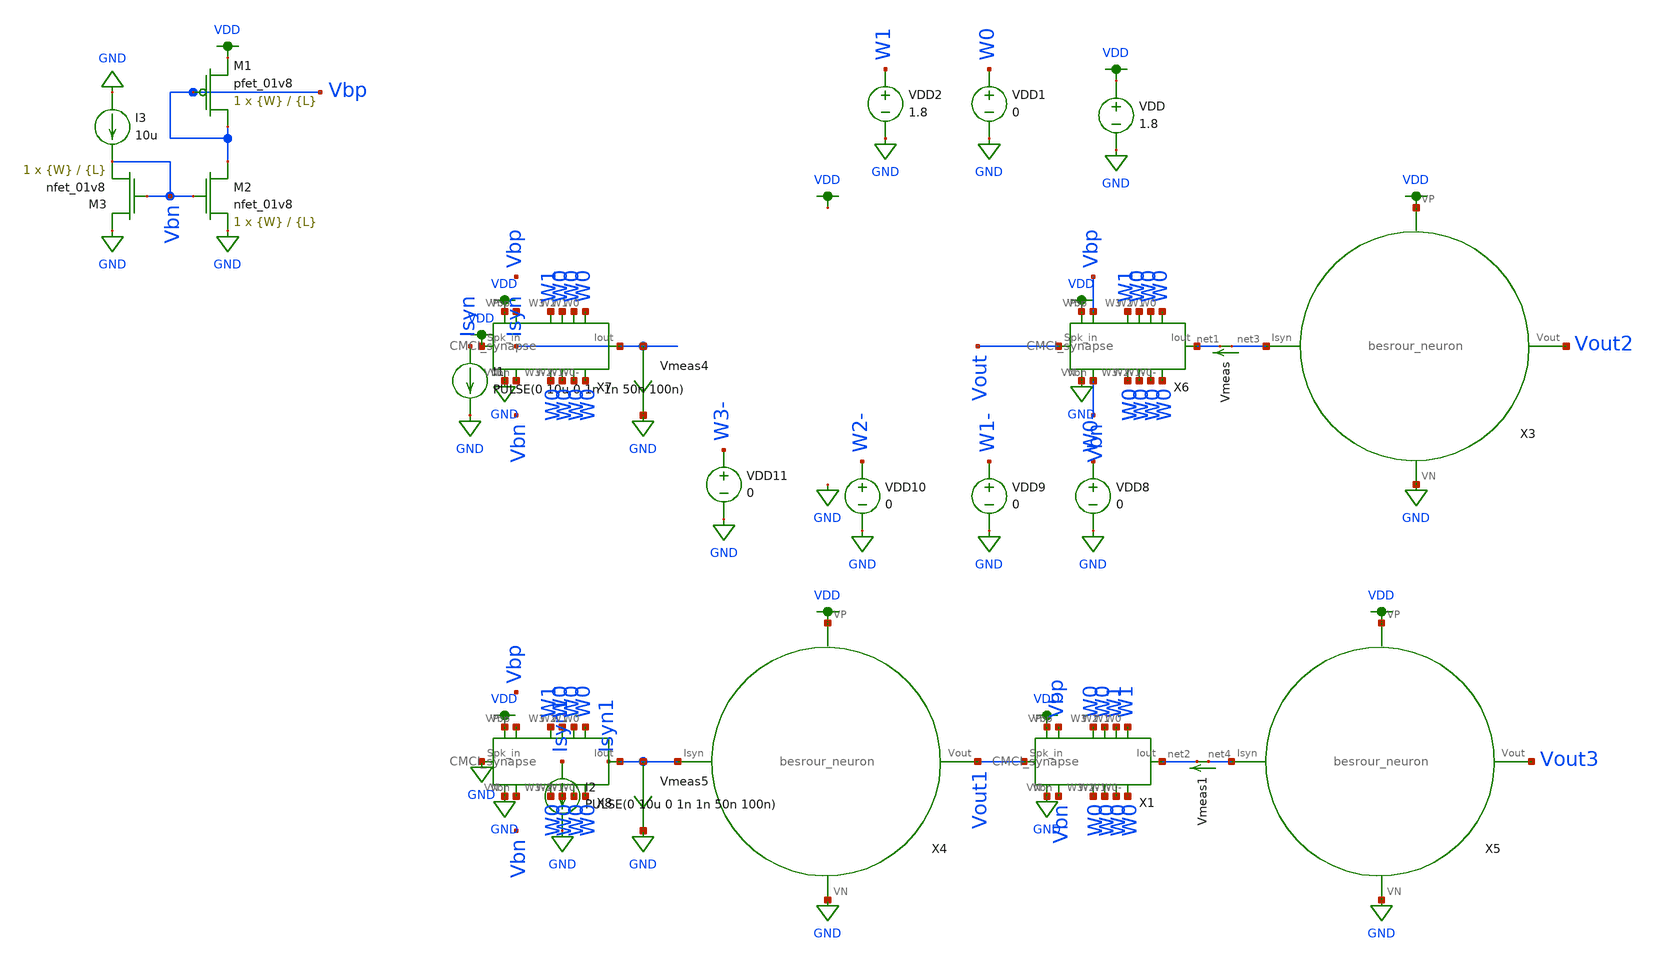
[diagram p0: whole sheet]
** sch_path: schematic/tran_besrour_CMCI.sch
**.subckt tran_besrour_CMCI
X4 Isyn1 Vout1 VDD GND besrour_neuron
VDD VDD GND 1.8
VDD1 W0 GND 0
VDD2 W1 GND 1.8
XM1 Vbp Vbp VDD VDD sky130_fd_pr__pfet_01v8 L={L} W={W} nf=1 ad='int((nf+1)/2) * W/nf * 0.29' as='int((nf+2)/2) * W/nf * 0.29'
+ pd='2*int((nf+1)/2) * (W/nf + 0.29)' ps='2*int((nf+2)/2) * (W/nf + 0.29)' nrd='0.29 / W' nrs='0.29 / W'
+ sa=0 sb=0 sd=0 mult=1 m=1
XM2 Vbp Vbn GND GND sky130_fd_pr__nfet_01v8 L={L} W={W} nf=1 ad='int((nf+1)/2) * W/nf * 0.29' as='int((nf+2)/2) * W/nf * 0.29'
+ pd='2*int((nf+1)/2) * (W/nf + 0.29)' ps='2*int((nf+2)/2) * (W/nf + 0.29)' nrd='0.29 / W' nrs='0.29 / W'
+ sa=0 sb=0 sd=0 mult=1 m=1
XM3 GND Vbn Vbn GND sky130_fd_pr__nfet_01v8 L={L} W={W} nf=1 ad='int((nf+1)/2) * W/nf * 0.29' as='int((nf+2)/2) * W/nf * 0.29'
+ pd='2*int((nf+1)/2) * (W/nf + 0.29)' ps='2*int((nf+2)/2) * (W/nf + 0.29)' nrd='0.29 / W' nrs='0.29 / W'
+ sa=0 sb=0 sd=0 mult=1 m=1
I3 GND Vbn 10u
X3 net3 Vout2 VDD GND besrour_neuron
X5 net4 Vout3 VDD GND besrour_neuron
X6 VDD Vbp W1 W0 W0 W0 net1 W0 W0 W0 W0 Vbn GND Vout CMCI_synapse
X1 VDD Vbp W0 W0 W1 W1 net2 W0 W0 W0 W0 Vbn GND Vout1 CMCI_synapse
I1 Isyn GND PULSE(0 10u 0 1n 1n 50n 100n)
I2 Isyn1 GND PULSE(0 10u 0 1n 1n 50n 100n)
Vmeas net3 net1 0
.save i(vmeas)
Vmeas1 net4 net2 0
.save i(vmeas1)
Vmeas4 Isyn GND 0
.save i(vmeas4)
X7 VDD net5 W1 W0 W0 W0 Isyn W0 W0 W0 W0 net6 GND VDD CMCI_synapse
Vmeas5 Isyn1 GND 0
.save i(vmeas5)
X8 VDD net7 W1 W0 W0 W0 Isyn1 W0 W0 W0 W0 net8 GND GND CMCI_synapse
VDD8 W0- GND 0
VDD9 W1- GND 0
VDD10 W2- GND 0
VDD11 W3- GND 0
**** begin user architecture code

.param W=1
.param L=0.15
.tran 0.1n 250n
.save all


.option wnflag=1
.param MC_SWITCH=0.0
.lib ~/skywater/skywater-pdk/libraries/sky130_fd_pr_ngspice/latest/models/sky130.lib.spice tt

**** end user architecture code
**.ends
.GLOBAL VDD
.GLOBAL GND
.end
